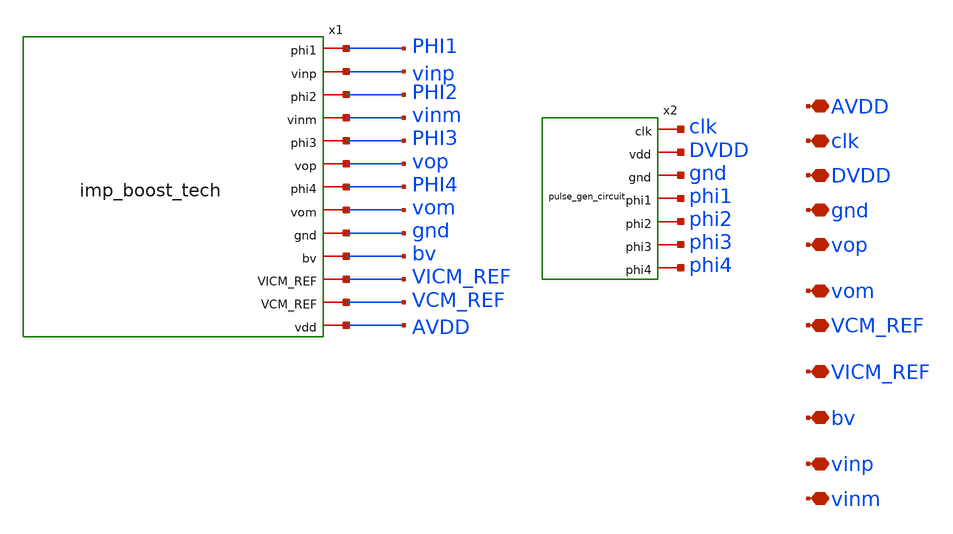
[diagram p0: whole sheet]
** sch_path: dependencies/OTA/OTA-main/schematic/xschem/digital_pulse_ina_temp_TOP.sch
**.subckt digital_pulse_ina_temp_TOP clk DVDD gnd vop vom VCM_REF VICM_REF bv vinp vinm AVDD
*.iopin clk
*.iopin DVDD
*.iopin gnd
*.iopin vop
*.iopin vom
*.iopin VCM_REF
*.iopin VICM_REF
*.iopin bv
*.iopin vinp
*.iopin vinm
*.iopin AVDD
x1 PHI1 vinp PHI2 vinm PHI3 vop PHI4 vom gnd bv VICM_REF VCM_REF AVDD imp_boost_tech
x2 clk DVDD gnd phi1 phi2 phi3 phi4 pulse_gen_circuit
**.ends
.end
